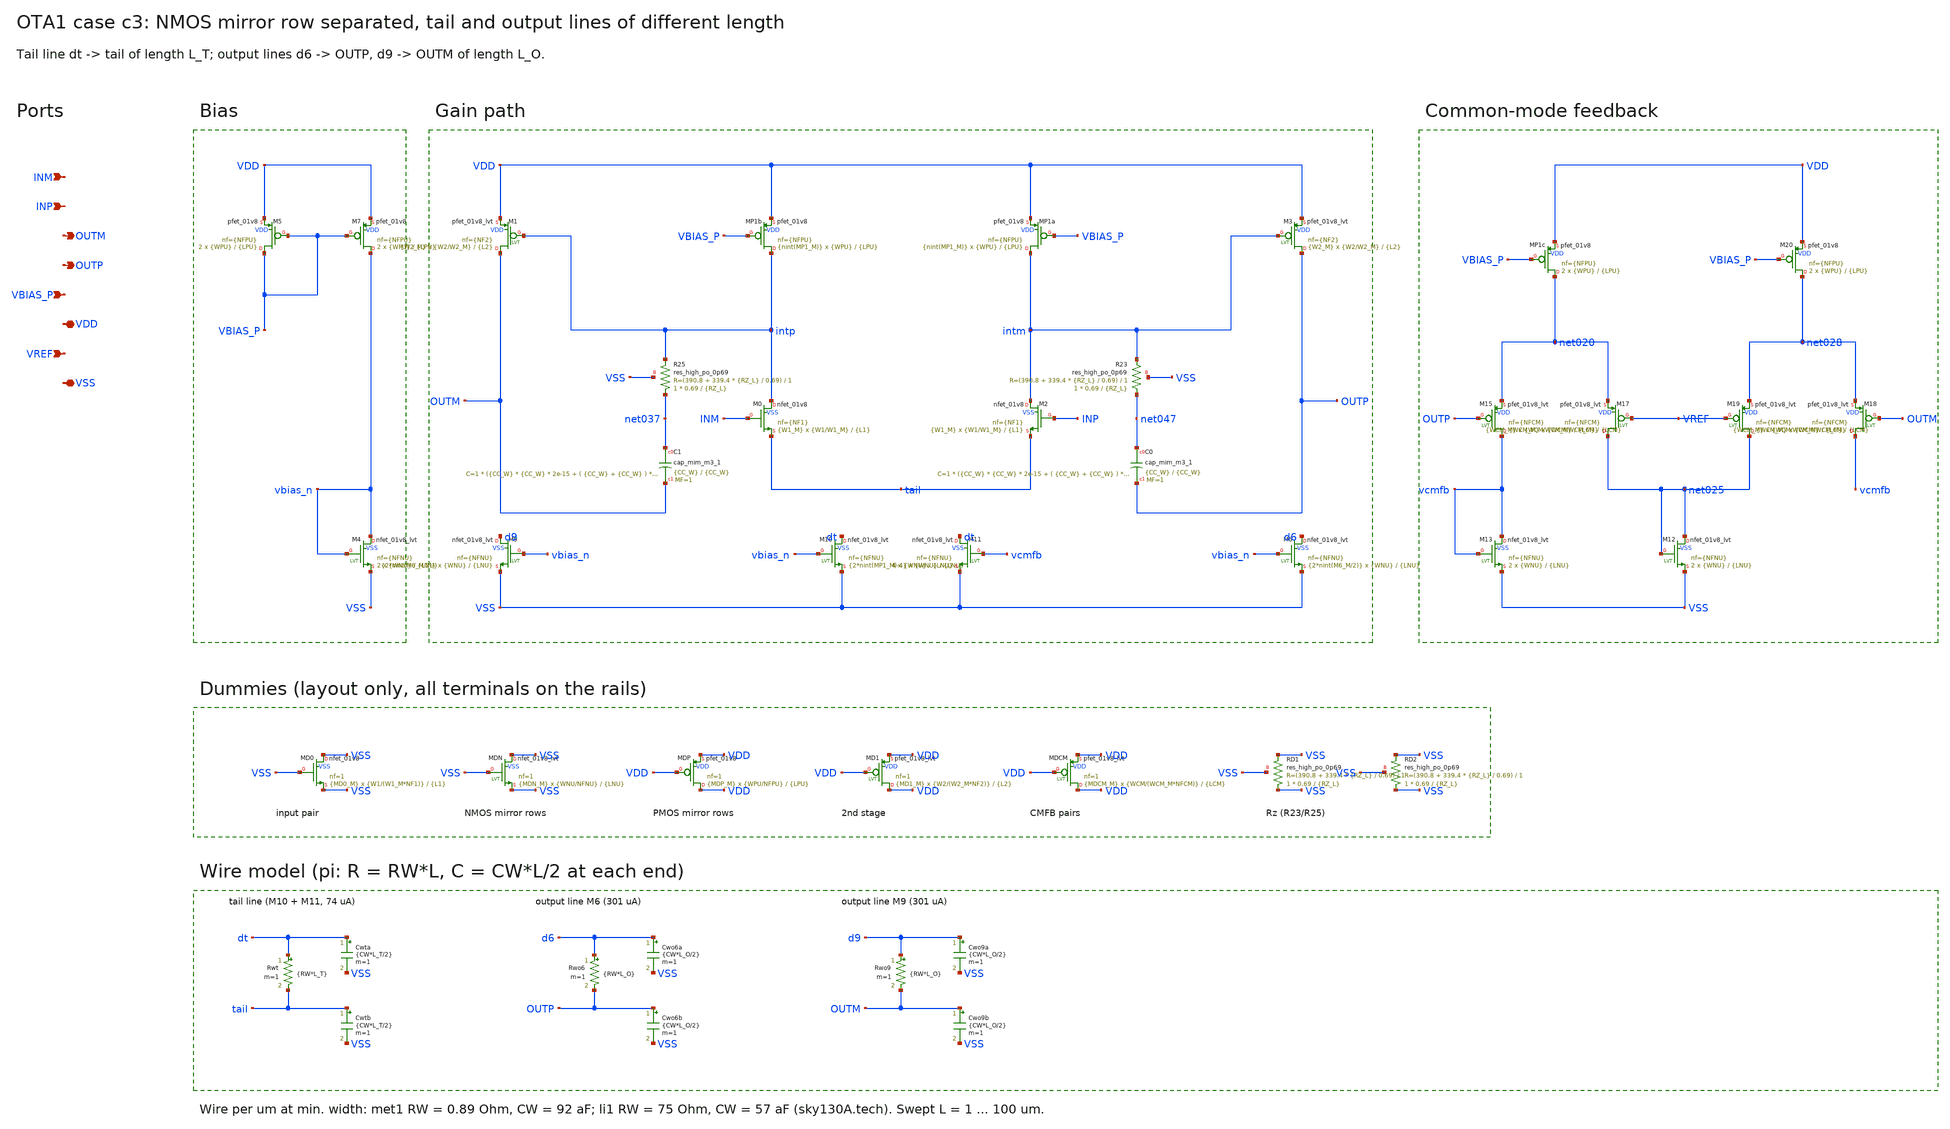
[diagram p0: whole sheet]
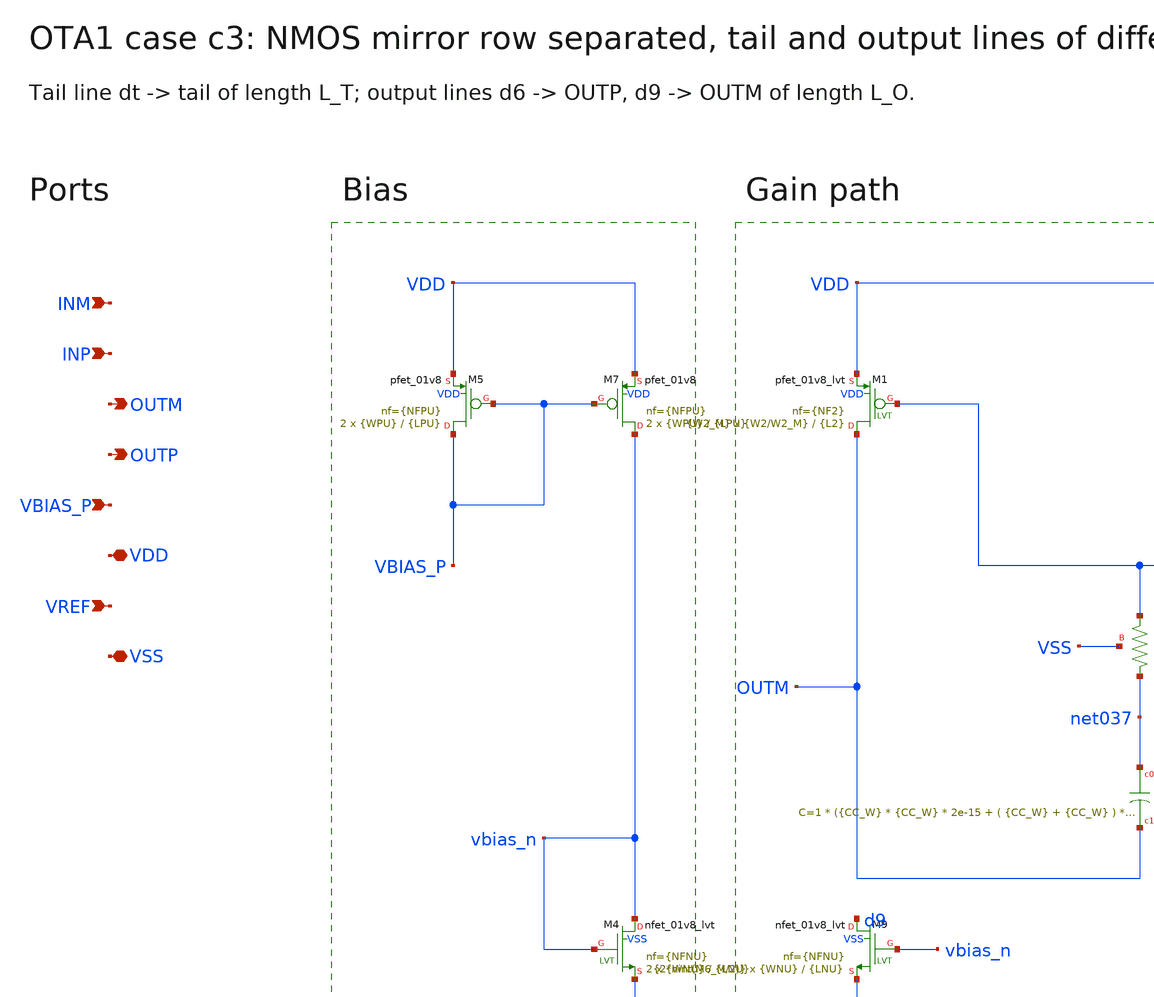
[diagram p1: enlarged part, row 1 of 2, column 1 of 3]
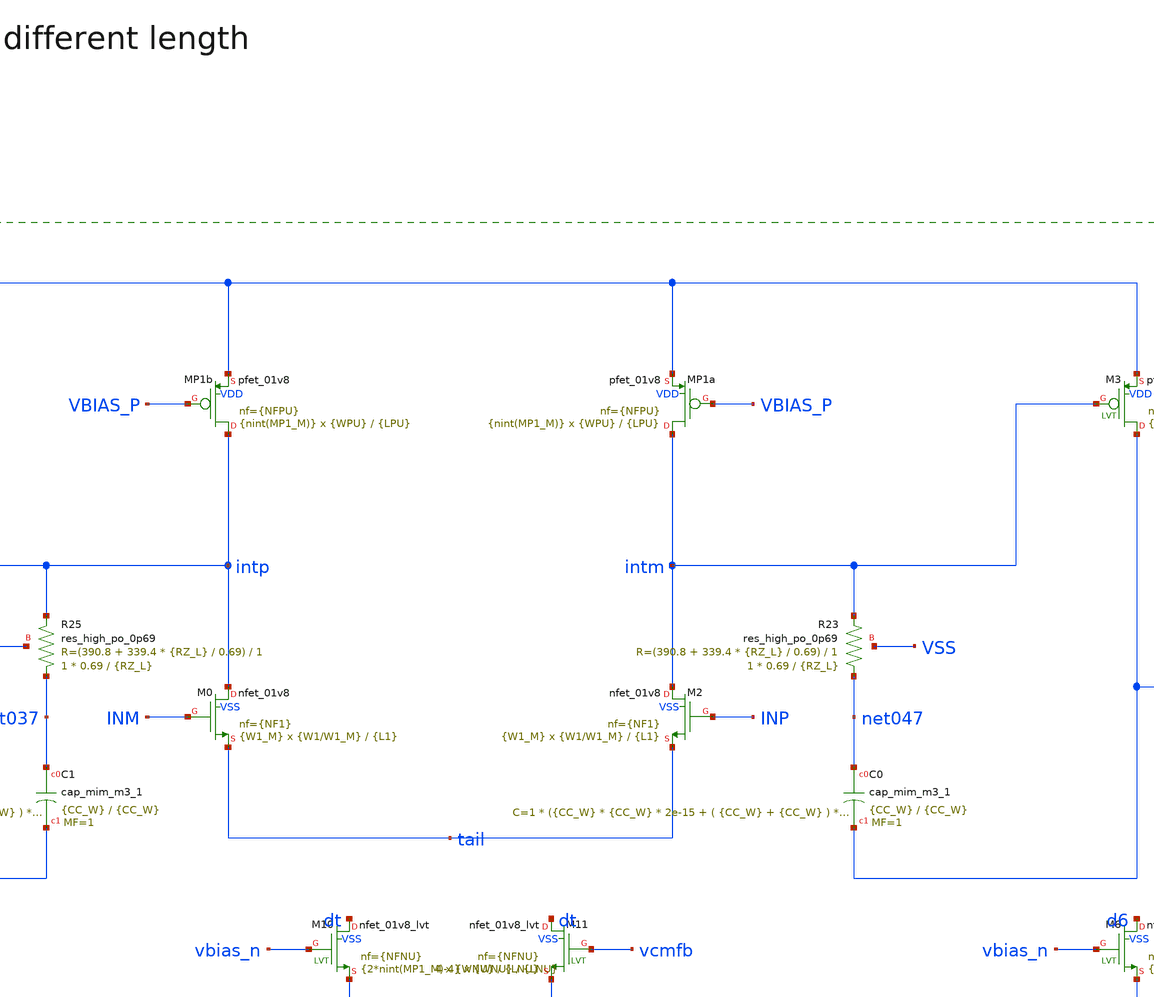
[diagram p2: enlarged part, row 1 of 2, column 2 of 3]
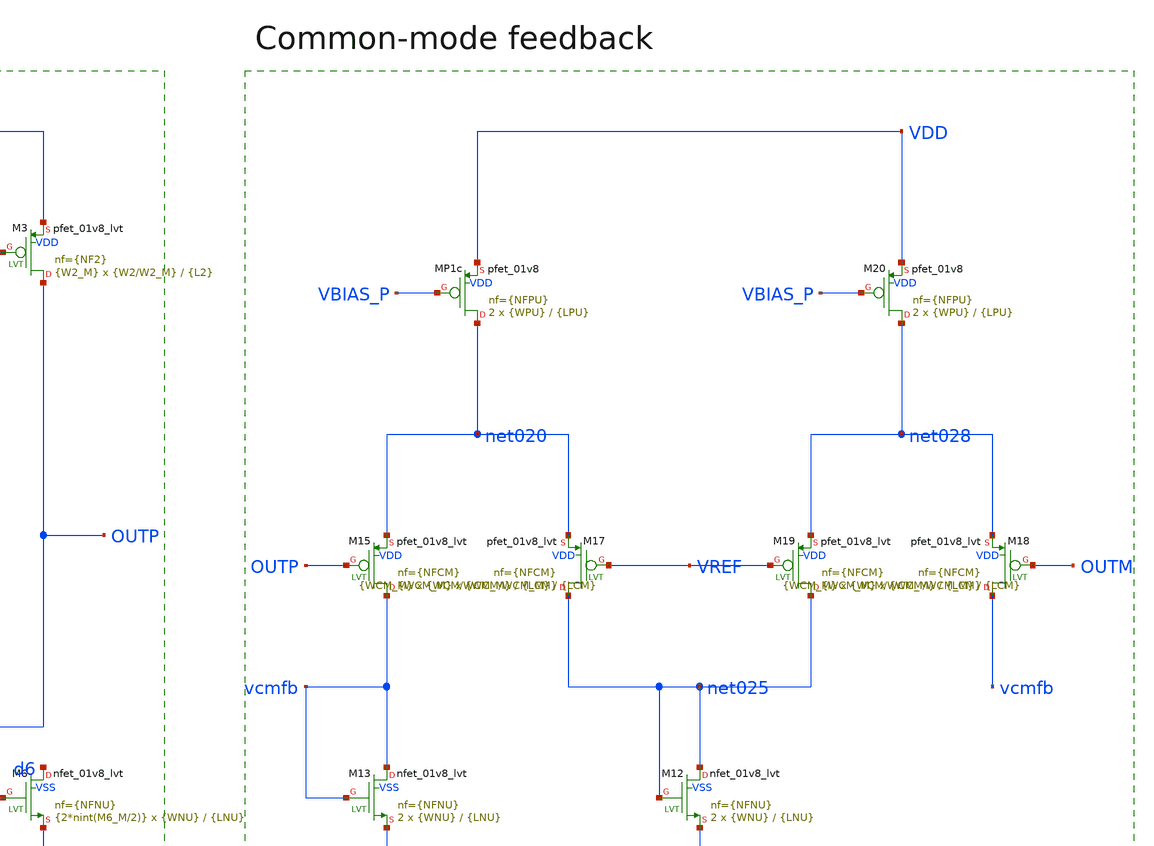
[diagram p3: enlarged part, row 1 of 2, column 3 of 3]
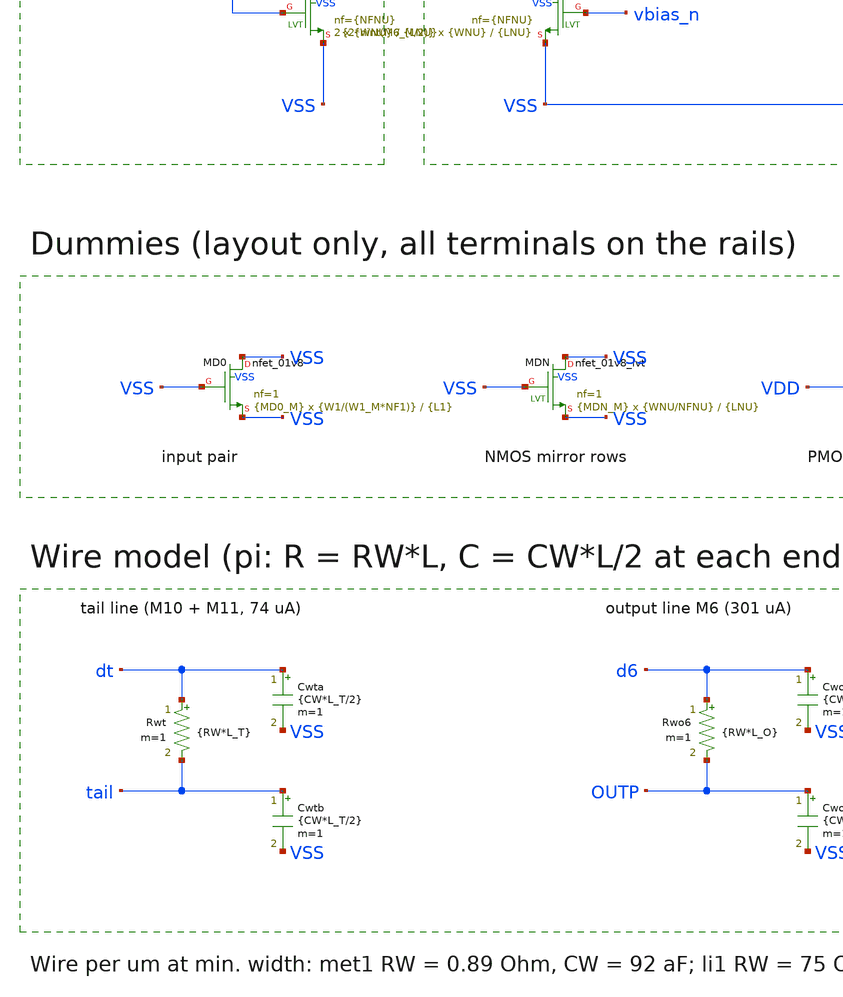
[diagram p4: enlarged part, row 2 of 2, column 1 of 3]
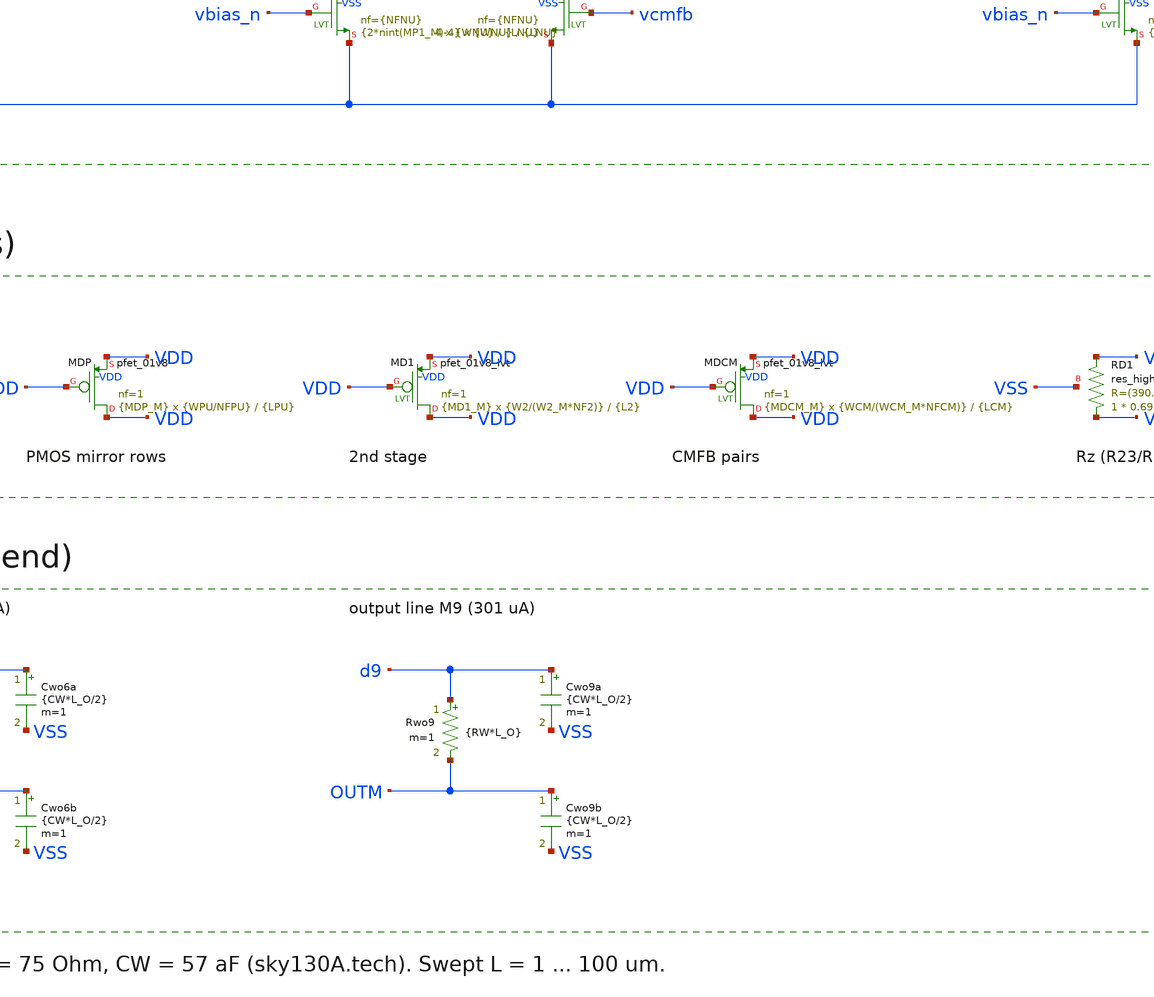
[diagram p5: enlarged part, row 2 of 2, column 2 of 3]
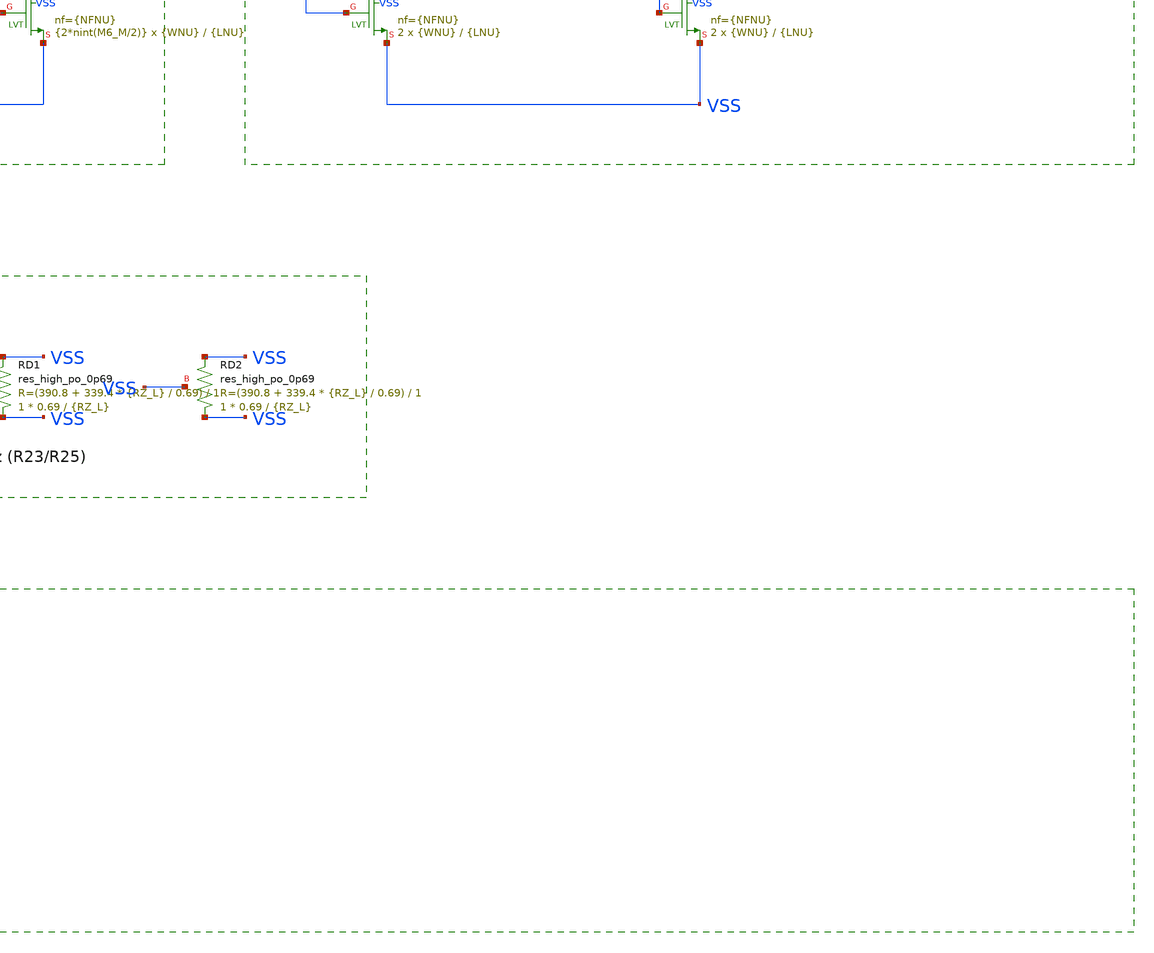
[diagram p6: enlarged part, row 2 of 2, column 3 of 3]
** sch_path: WorkDir/experiments/cm_separation/ota1_c3.sch
**.subckt ota1_c3 INM INP OUTM OUTP VBIAS_P VDD VREF VSS
*.ipin INM
*.ipin INP
*.opin OUTM
*.opin OUTP
*.ipin VBIAS_P
*.iopin VDD
*.ipin VREF
*.iopin VSS
XMP1b intp VBIAS_P VDD VDD sky130_fd_pr__pfet_01v8 L={LPU} W={WPU} nf={NFPU} ad='int(({NFPU} + 1)/2) * {WPU} / {NFPU} * 0.29'
+ as='int(({NFPU} + 2)/2) * {WPU} / {NFPU} * 0.29' pd='2*int(({NFPU} + 1)/2) * ({WPU} / {NFPU} + 0.29)'
+ ps='2*int(({NFPU} + 2)/2) * ({WPU} / {NFPU} + 0.29)' nrd='0.29 / {WPU} ' nrs='0.29 / {WPU} ' sa=0 sb=0
+ sd=0 mult={nint(MP1_M)} m={nint(MP1_M)}
XM0 intp INM tail VSS sky130_fd_pr__nfet_01v8 L={L1} W={W1/W1_M} nf={NF1} ad='int(({NF1} + 1)/2) * {W1/W1_M} / {NF1} * 0.29'
+ as='int(({NF1} + 2)/2) * {W1/W1_M} / {NF1} * 0.29' pd='2*int(({NF1} + 1)/2) * ({W1/W1_M} / {NF1} + 0.29)'
+ ps='2*int(({NF1} + 2)/2) * ({W1/W1_M} / {NF1} + 0.29)' nrd='0.29 / {W1/W1_M} ' nrs='0.29 / {W1/W1_M} '
+ sa=0 sb=0 sd=0 mult={W1_M} m={W1_M}
XM1 OUTM intp VDD VDD sky130_fd_pr__pfet_01v8_lvt L={L2} W={W2/W2_M} nf={NF2} ad='int(({NF2} + 1)/2) * {W2/W2_M} / {NF2} * 0.29'
+ as='int(({NF2} + 2)/2) * {W2/W2_M} / {NF2} * 0.29' pd='2*int(({NF2} + 1)/2) * ({W2/W2_M} / {NF2} + 0.29)'
+ ps='2*int(({NF2} + 2)/2) * ({W2/W2_M} / {NF2} + 0.29)' nrd='0.29 / {W2/W2_M} ' nrs='0.29 / {W2/W2_M} '
+ sa=0 sb=0 sd=0 mult={W2_M} m={W2_M}
XM9 d9 vbias_n VSS VSS sky130_fd_pr__nfet_01v8_lvt L={LNU} W={WNU} nf={NFNU} ad='int(({NFNU} + 1)/2) * {WNU} / {NFNU} * 0.29'
+ as='int(({NFNU} + 2)/2) * {WNU} / {NFNU} * 0.29' pd='2*int(({NFNU} + 1)/2) * ({WNU} / {NFNU} + 0.29)'
+ ps='2*int(({NFNU} + 2)/2) * ({WNU} / {NFNU} + 0.29)' nrd='0.29 / {WNU} ' nrs='0.29 / {WNU} ' sa=0 sb=0
+ sd=0 mult={2*nint(M6_M/2)} m={2*nint(M6_M/2)}
XR25 net037 intp VSS sky130_fd_pr__res_high_po_0p69 L={RZ_L} mult=1 m=1
XC1 net037 OUTM sky130_fd_pr__cap_mim_m3_1 W={CC_W} L={CC_W} MF=1 m=1
XMP1a intm VBIAS_P VDD VDD sky130_fd_pr__pfet_01v8 L={LPU} W={WPU} nf={NFPU} ad='int(({NFPU} + 1)/2) * {WPU} / {NFPU} * 0.29'
+ as='int(({NFPU} + 2)/2) * {WPU} / {NFPU} * 0.29' pd='2*int(({NFPU} + 1)/2) * ({WPU} / {NFPU} + 0.29)'
+ ps='2*int(({NFPU} + 2)/2) * ({WPU} / {NFPU} + 0.29)' nrd='0.29 / {WPU} ' nrs='0.29 / {WPU} ' sa=0 sb=0
+ sd=0 mult={nint(MP1_M)} m={nint(MP1_M)}
XM2 intm INP tail VSS sky130_fd_pr__nfet_01v8 L={L1} W={W1/W1_M} nf={NF1} ad='int(({NF1} + 1)/2) * {W1/W1_M} / {NF1} * 0.29'
+ as='int(({NF1} + 2)/2) * {W1/W1_M} / {NF1} * 0.29' pd='2*int(({NF1} + 1)/2) * ({W1/W1_M} / {NF1} + 0.29)'
+ ps='2*int(({NF1} + 2)/2) * ({W1/W1_M} / {NF1} + 0.29)' nrd='0.29 / {W1/W1_M} ' nrs='0.29 / {W1/W1_M} '
+ sa=0 sb=0 sd=0 mult={W1_M} m={W1_M}
XM3 OUTP intm VDD VDD sky130_fd_pr__pfet_01v8_lvt L={L2} W={W2/W2_M} nf={NF2} ad='int(({NF2} + 1)/2) * {W2/W2_M} / {NF2} * 0.29'
+ as='int(({NF2} + 2)/2) * {W2/W2_M} / {NF2} * 0.29' pd='2*int(({NF2} + 1)/2) * ({W2/W2_M} / {NF2} + 0.29)'
+ ps='2*int(({NF2} + 2)/2) * ({W2/W2_M} / {NF2} + 0.29)' nrd='0.29 / {W2/W2_M} ' nrs='0.29 / {W2/W2_M} '
+ sa=0 sb=0 sd=0 mult={W2_M} m={W2_M}
XM6 d6 vbias_n VSS VSS sky130_fd_pr__nfet_01v8_lvt L={LNU} W={WNU} nf={NFNU} ad='int(({NFNU} + 1)/2) * {WNU} / {NFNU} * 0.29'
+ as='int(({NFNU} + 2)/2) * {WNU} / {NFNU} * 0.29' pd='2*int(({NFNU} + 1)/2) * ({WNU} / {NFNU} + 0.29)'
+ ps='2*int(({NFNU} + 2)/2) * ({WNU} / {NFNU} + 0.29)' nrd='0.29 / {WNU} ' nrs='0.29 / {WNU} ' sa=0 sb=0
+ sd=0 mult={2*nint(M6_M/2)} m={2*nint(M6_M/2)}
XR23 net047 intm VSS sky130_fd_pr__res_high_po_0p69 L={RZ_L} mult=1 m=1
XC0 net047 OUTP sky130_fd_pr__cap_mim_m3_1 W={CC_W} L={CC_W} MF=1 m=1
XM10 dt vbias_n VSS VSS sky130_fd_pr__nfet_01v8_lvt L={LNU} W={WNU} nf={NFNU} ad='int(({NFNU} + 1)/2) * {WNU} / {NFNU} * 0.29'
+ as='int(({NFNU} + 2)/2) * {WNU} / {NFNU} * 0.29' pd='2*int(({NFNU} + 1)/2) * ({WNU} / {NFNU} + 0.29)'
+ ps='2*int(({NFNU} + 2)/2) * ({WNU} / {NFNU} + 0.29)' nrd='0.29 / {WNU} ' nrs='0.29 / {WNU} ' sa=0 sb=0
+ sd=0 mult={2*nint(MP1_M)-4} m={2*nint(MP1_M)-4}
XM11 dt vcmfb VSS VSS sky130_fd_pr__nfet_01v8_lvt L={LNU} W={WNU} nf={NFNU} ad='int(({NFNU} + 1)/2) * {WNU} / {NFNU} * 0.29'
+ as='int(({NFNU} + 2)/2) * {WNU} / {NFNU} * 0.29' pd='2*int(({NFNU} + 1)/2) * ({WNU} / {NFNU} + 0.29)'
+ ps='2*int(({NFNU} + 2)/2) * ({WNU} / {NFNU} + 0.29)' nrd='0.29 / {WNU} ' nrs='0.29 / {WNU} ' sa=0 sb=0
+ sd=0 mult=4 m=4
XM5 VBIAS_P VBIAS_P VDD VDD sky130_fd_pr__pfet_01v8 L={LPU} W={WPU} nf={NFPU} ad='int(({NFPU} + 1)/2) * {WPU} / {NFPU} * 0.29'
+ as='int(({NFPU} + 2)/2) * {WPU} / {NFPU} * 0.29' pd='2*int(({NFPU} + 1)/2) * ({WPU} / {NFPU} + 0.29)'
+ ps='2*int(({NFPU} + 2)/2) * ({WPU} / {NFPU} + 0.29)' nrd='0.29 / {WPU} ' nrs='0.29 / {WPU} ' sa=0 sb=0
+ sd=0 mult=2 m=2
XM7 vbias_n VBIAS_P VDD VDD sky130_fd_pr__pfet_01v8 L={LPU} W={WPU} nf={NFPU} ad='int(({NFPU} + 1)/2) * {WPU} / {NFPU} * 0.29'
+ as='int(({NFPU} + 2)/2) * {WPU} / {NFPU} * 0.29' pd='2*int(({NFPU} + 1)/2) * ({WPU} / {NFPU} + 0.29)'
+ ps='2*int(({NFPU} + 2)/2) * ({WPU} / {NFPU} + 0.29)' nrd='0.29 / {WPU} ' nrs='0.29 / {WPU} ' sa=0 sb=0
+ sd=0 mult=2 m=2
XM4 vbias_n vbias_n VSS VSS sky130_fd_pr__nfet_01v8_lvt L={LNU} W={WNU} nf={NFNU} ad='int(({NFNU} + 1)/2) * {WNU} / {NFNU} * 0.29'
+ as='int(({NFNU} + 2)/2) * {WNU} / {NFNU} * 0.29' pd='2*int(({NFNU} + 1)/2) * ({WNU} / {NFNU} + 0.29)'
+ ps='2*int(({NFNU} + 2)/2) * ({WNU} / {NFNU} + 0.29)' nrd='0.29 / {WNU} ' nrs='0.29 / {WNU} ' sa=0 sb=0
+ sd=0 mult=2 m=2
XM15 vcmfb OUTP net020 VDD sky130_fd_pr__pfet_01v8_lvt L={LCM} W={WCM/WCM_M} nf={NFCM} ad='int(({NFCM} + 1)/2) * {WCM/WCM_M} / {NFCM} * 0.29'
+ as='int(({NFCM} + 2)/2) * {WCM/WCM_M} / {NFCM} * 0.29' pd='2*int(({NFCM} + 1)/2) * ({WCM/WCM_M} / {NFCM} + 0.29)'
+ ps='2*int(({NFCM} + 2)/2) * ({WCM/WCM_M} / {NFCM} + 0.29)' nrd='0.29 / {WCM/WCM_M} ' nrs='0.29 / {WCM/WCM_M} '
+ sa=0 sb=0 sd=0 mult={WCM_M} m={WCM_M}
XM17 net025 VREF net020 VDD sky130_fd_pr__pfet_01v8_lvt L={LCM} W={WCM/WCM_M} nf={NFCM} ad='int(({NFCM} + 1)/2) * {WCM/WCM_M} / {NFCM} * 0.29'
+ as='int(({NFCM} + 2)/2) * {WCM/WCM_M} / {NFCM} * 0.29' pd='2*int(({NFCM} + 1)/2) * ({WCM/WCM_M} / {NFCM} + 0.29)'
+ ps='2*int(({NFCM} + 2)/2) * ({WCM/WCM_M} / {NFCM} + 0.29)' nrd='0.29 / {WCM/WCM_M} ' nrs='0.29 / {WCM/WCM_M} '
+ sa=0 sb=0 sd=0 mult={WCM_M} m={WCM_M}
XM19 net025 VREF net028 VDD sky130_fd_pr__pfet_01v8_lvt L={LCM} W={WCM/WCM_M} nf={NFCM} ad='int(({NFCM} + 1)/2) * {WCM/WCM_M} / {NFCM} * 0.29'
+ as='int(({NFCM} + 2)/2) * {WCM/WCM_M} / {NFCM} * 0.29' pd='2*int(({NFCM} + 1)/2) * ({WCM/WCM_M} / {NFCM} + 0.29)'
+ ps='2*int(({NFCM} + 2)/2) * ({WCM/WCM_M} / {NFCM} + 0.29)' nrd='0.29 / {WCM/WCM_M} ' nrs='0.29 / {WCM/WCM_M} '
+ sa=0 sb=0 sd=0 mult={WCM_M} m={WCM_M}
XM18 vcmfb OUTM net028 VDD sky130_fd_pr__pfet_01v8_lvt L={LCM} W={WCM/WCM_M} nf={NFCM} ad='int(({NFCM} + 1)/2) * {WCM/WCM_M} / {NFCM} * 0.29'
+ as='int(({NFCM} + 2)/2) * {WCM/WCM_M} / {NFCM} * 0.29' pd='2*int(({NFCM} + 1)/2) * ({WCM/WCM_M} / {NFCM} + 0.29)'
+ ps='2*int(({NFCM} + 2)/2) * ({WCM/WCM_M} / {NFCM} + 0.29)' nrd='0.29 / {WCM/WCM_M} ' nrs='0.29 / {WCM/WCM_M} '
+ sa=0 sb=0 sd=0 mult={WCM_M} m={WCM_M}
XMP1c net020 VBIAS_P VDD VDD sky130_fd_pr__pfet_01v8 L={LPU} W={WPU} nf={NFPU} ad='int(({NFPU} + 1)/2) * {WPU} / {NFPU} * 0.29'
+ as='int(({NFPU} + 2)/2) * {WPU} / {NFPU} * 0.29' pd='2*int(({NFPU} + 1)/2) * ({WPU} / {NFPU} + 0.29)'
+ ps='2*int(({NFPU} + 2)/2) * ({WPU} / {NFPU} + 0.29)' nrd='0.29 / {WPU} ' nrs='0.29 / {WPU} ' sa=0 sb=0
+ sd=0 mult=2 m=2
XM20 net028 VBIAS_P VDD VDD sky130_fd_pr__pfet_01v8 L={LPU} W={WPU} nf={NFPU} ad='int(({NFPU} + 1)/2) * {WPU} / {NFPU} * 0.29'
+ as='int(({NFPU} + 2)/2) * {WPU} / {NFPU} * 0.29' pd='2*int(({NFPU} + 1)/2) * ({WPU} / {NFPU} + 0.29)'
+ ps='2*int(({NFPU} + 2)/2) * ({WPU} / {NFPU} + 0.29)' nrd='0.29 / {WPU} ' nrs='0.29 / {WPU} ' sa=0 sb=0
+ sd=0 mult=2 m=2
XM13 vcmfb vcmfb VSS VSS sky130_fd_pr__nfet_01v8_lvt L={LNU} W={WNU} nf={NFNU} ad='int(({NFNU} + 1)/2) * {WNU} / {NFNU} * 0.29'
+ as='int(({NFNU} + 2)/2) * {WNU} / {NFNU} * 0.29' pd='2*int(({NFNU} + 1)/2) * ({WNU} / {NFNU} + 0.29)'
+ ps='2*int(({NFNU} + 2)/2) * ({WNU} / {NFNU} + 0.29)' nrd='0.29 / {WNU} ' nrs='0.29 / {WNU} ' sa=0 sb=0
+ sd=0 mult=2 m=2
XM12 net025 net025 VSS VSS sky130_fd_pr__nfet_01v8_lvt L={LNU} W={WNU} nf={NFNU} ad='int(({NFNU} + 1)/2) * {WNU} / {NFNU} * 0.29'
+ as='int(({NFNU} + 2)/2) * {WNU} / {NFNU} * 0.29' pd='2*int(({NFNU} + 1)/2) * ({WNU} / {NFNU} + 0.29)'
+ ps='2*int(({NFNU} + 2)/2) * ({WNU} / {NFNU} + 0.29)' nrd='0.29 / {WNU} ' nrs='0.29 / {WNU} ' sa=0 sb=0
+ sd=0 mult=2 m=2
XMD0 VSS VSS VSS VSS sky130_fd_pr__nfet_01v8 L={L1} W={W1/(W1_M*NF1)} nf=1 ad='int((1 + 1)/2) * {W1/(W1_M*NF1)} / 1 * 0.29'
+ as='int((1 + 2)/2) * {W1/(W1_M*NF1)} / 1 * 0.29' pd='2*int((1 + 1)/2) * ({W1/(W1_M*NF1)} / 1 + 0.29)'
+ ps='2*int((1 + 2)/2) * ({W1/(W1_M*NF1)} / 1 + 0.29)' nrd='0.29 / {W1/(W1_M*NF1)} ' nrs='0.29 / {W1/(W1_M*NF1)} '
+ sa=0 sb=0 sd=0 mult={MD0_M} m={MD0_M}
XMDN VSS VSS VSS VSS sky130_fd_pr__nfet_01v8_lvt L={LNU} W={WNU/NFNU} nf=1 ad='int((1 + 1)/2) * {WNU/NFNU} / 1 * 0.29'
+ as='int((1 + 2)/2) * {WNU/NFNU} / 1 * 0.29' pd='2*int((1 + 1)/2) * ({WNU/NFNU} / 1 + 0.29)' ps='2*int((1 + 2)/2) * ({WNU/NFNU} / 1 + 0.29)'
+ nrd='0.29 / {WNU/NFNU} ' nrs='0.29 / {WNU/NFNU} ' sa=0 sb=0 sd=0 mult={MDN_M} m={MDN_M}
XMDP VDD VDD VDD VDD sky130_fd_pr__pfet_01v8 L={LPU} W={WPU/NFPU} nf=1 ad='int((1 + 1)/2) * {WPU/NFPU} / 1 * 0.29'
+ as='int((1 + 2)/2) * {WPU/NFPU} / 1 * 0.29' pd='2*int((1 + 1)/2) * ({WPU/NFPU} / 1 + 0.29)' ps='2*int((1 + 2)/2) * ({WPU/NFPU} / 1 + 0.29)'
+ nrd='0.29 / {WPU/NFPU} ' nrs='0.29 / {WPU/NFPU} ' sa=0 sb=0 sd=0 mult={MDP_M} m={MDP_M}
XMD1 VDD VDD VDD VDD sky130_fd_pr__pfet_01v8_lvt L={L2} W={W2/(W2_M*NF2)} nf=1 ad='int((1 + 1)/2) * {W2/(W2_M*NF2)} / 1 * 0.29'
+ as='int((1 + 2)/2) * {W2/(W2_M*NF2)} / 1 * 0.29' pd='2*int((1 + 1)/2) * ({W2/(W2_M*NF2)} / 1 + 0.29)'
+ ps='2*int((1 + 2)/2) * ({W2/(W2_M*NF2)} / 1 + 0.29)' nrd='0.29 / {W2/(W2_M*NF2)} ' nrs='0.29 / {W2/(W2_M*NF2)} '
+ sa=0 sb=0 sd=0 mult={MD1_M} m={MD1_M}
XMDCM VDD VDD VDD VDD sky130_fd_pr__pfet_01v8_lvt L={LCM} W={WCM/(WCM_M*NFCM)} nf=1 ad='int((1 + 1)/2) * {WCM/(WCM_M*NFCM)} / 1 * 0.29'
+ as='int((1 + 2)/2) * {WCM/(WCM_M*NFCM)} / 1 * 0.29' pd='2*int((1 + 1)/2) * ({WCM/(WCM_M*NFCM)} / 1 + 0.29)'
+ ps='2*int((1 + 2)/2) * ({WCM/(WCM_M*NFCM)} / 1 + 0.29)' nrd='0.29 / {WCM/(WCM_M*NFCM)} ' nrs='0.29 / {WCM/(WCM_M*NFCM)} '
+ sa=0 sb=0 sd=0 mult={MDCM_M} m={MDCM_M}
XRD1 VSS VSS VSS sky130_fd_pr__res_high_po_0p69 L={RZ_L} mult=1 m=1
XRD2 VSS VSS VSS sky130_fd_pr__res_high_po_0p69 L={RZ_L} mult=1 m=1
Rwt dt tail {RW*L_T} m=1
Cwta dt VSS {CW*L_T/2} m=1
Cwtb tail VSS {CW*L_T/2} m=1
Rwo6 d6 OUTP {RW*L_O} m=1
Cwo6a d6 VSS {CW*L_O/2} m=1
Cwo6b OUTP VSS {CW*L_O/2} m=1
Rwo9 d9 OUTM {RW*L_O} m=1
Cwo9a d9 VSS {CW*L_O/2} m=1
Cwo9b OUTM VSS {CW*L_O/2} m=1
**.ends
.end
